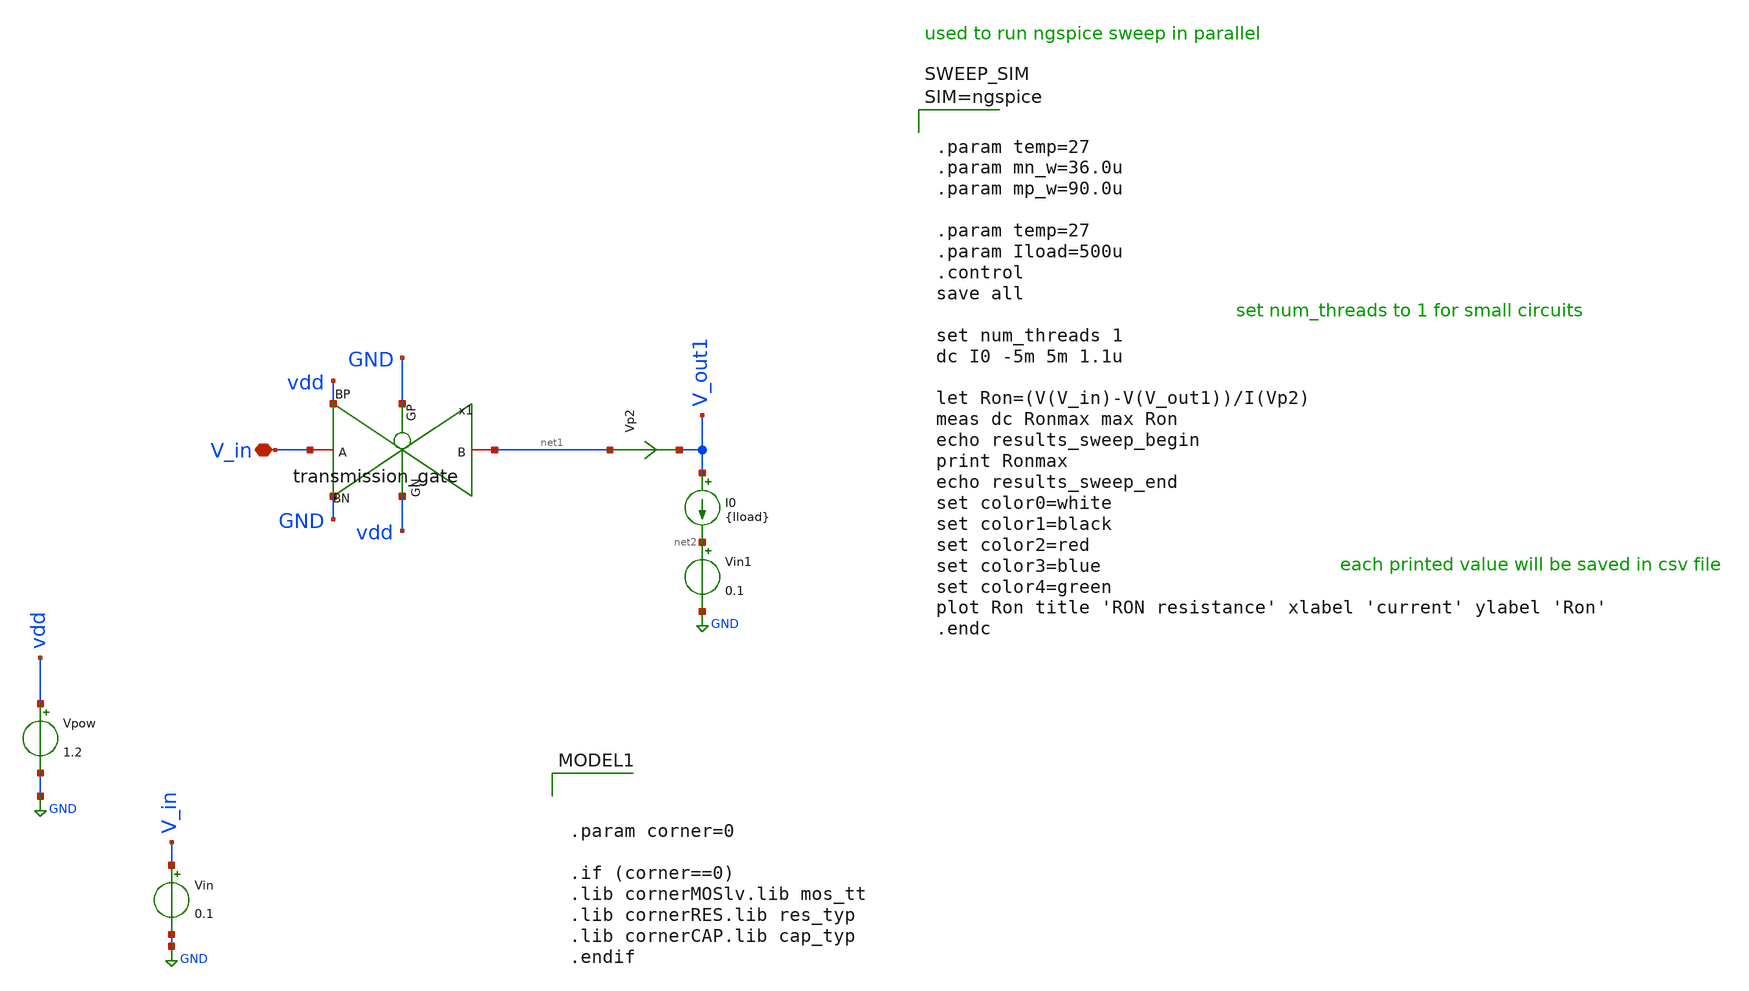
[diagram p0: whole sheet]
** sch_path: design_data/old/t-tb_gate_lv_isweep_chipathon.sch
**.subckt t-tb_gate_lv_isweep_chipathon V_in
*.iopin V_in
Vpow vdd GND 1.2
Vin V_in GND 0.1
I0 V_out1 net2 {Iload}
Vp2 net1 V_out1 0
.save i(vp2)
Vin1 net2 GND 0.1
x1 net1 vdd GND V_in vdd GND transmission_gate
**** begin user architecture code



.param temp=27
.param mn_w=36.0u
.param mp_w=90.0u

.param temp=27
.param Iload=500u
.control
save all

set num_threads 1
dc I0 -5m 5m 1.1u

let Ron=(V(V_in)-V(V_out1))/I(Vp2)
meas dc Ronmax max Ron
echo results_sweep_begin
print Ronmax
echo results_sweep_end
set color0=white
set color1=black
set color2=red
set color3=blue
set color4=green
plot Ron title 'RON resistance' xlabel 'current' ylabel 'Ron'
.endc





.param corner=0

.if (corner==0)
.lib cornerMOSlv.lib mos_tt
.lib cornerRES.lib res_typ
.lib cornerCAP.lib cap_typ
.endif

**** end user architecture code
**.ends

* expanding   symbol:  transmission_gate.sym # of pins=6
** sym_path: transmission_gate.sym
** sch_path: transmission_gate.sch
.subckt transmission_gate B GN GP A BP BN
*.iopin B
*.iopin GN
*.iopin A
*.iopin GP
*.iopin BN
*.iopin BP
XM1 A GN B BN sg13_lv_nmos w=10u l=0.13u ng=1 m=1 mm_ok=1
XM2 A GP B BP sg13_lv_pmos w=20u l=0.13u ng=2 m=1 mm_ok=1
.ends

.GLOBAL GND
.end
